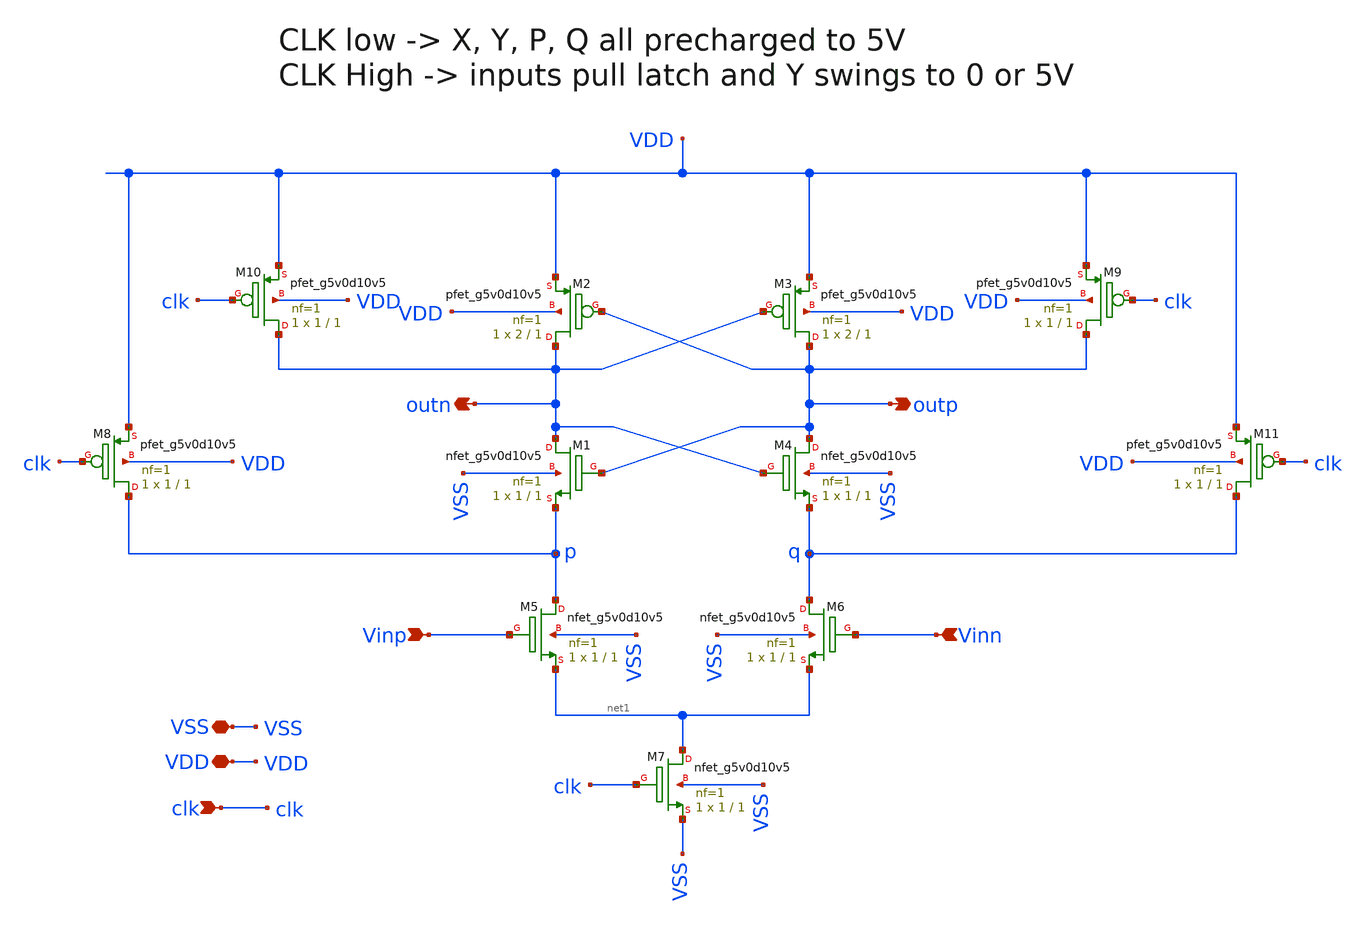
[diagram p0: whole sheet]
** sch_path: ADC/4bit_C2C/MagicAndSpice/strongarm_comp.sch
**.subckt strongarm_comp Vinp Vinn clk VDD outp outn VSS
*.ipin Vinp
*.ipin Vinn
*.ipin clk
*.iopin VDD
*.opin outp
*.opin outn
*.iopin VSS
XM1 outn outp p VSS sky130_fd_pr__nfet_g5v0d10v5 L=1 W=1 nf=1 ad='int((nf+1)/2) * W/nf * 0.29' as='int((nf+2)/2) * W/nf * 0.29'
+ pd='2*int((nf+1)/2) * (W/nf + 0.29)' ps='2*int((nf+2)/2) * (W/nf + 0.29)' nrd='0.29 / W' nrs='0.29 / W'
+ sa=0 sb=0 sd=0 mult=1 m=1
XM2 outn outp VDD VDD sky130_fd_pr__pfet_g5v0d10v5 L=1 W=2 nf=1 ad='int((nf+1)/2) * W/nf * 0.29' as='int((nf+2)/2) * W/nf * 0.29'
+ pd='2*int((nf+1)/2) * (W/nf + 0.29)' ps='2*int((nf+2)/2) * (W/nf + 0.29)' nrd='0.29 / W' nrs='0.29 / W'
+ sa=0 sb=0 sd=0 mult=1 m=1
XM3 outp outn VDD VDD sky130_fd_pr__pfet_g5v0d10v5 L=1 W=2 nf=1 ad='int((nf+1)/2) * W/nf * 0.29' as='int((nf+2)/2) * W/nf * 0.29'
+ pd='2*int((nf+1)/2) * (W/nf + 0.29)' ps='2*int((nf+2)/2) * (W/nf + 0.29)' nrd='0.29 / W' nrs='0.29 / W'
+ sa=0 sb=0 sd=0 mult=1 m=1
XM4 outp outn q VSS sky130_fd_pr__nfet_g5v0d10v5 L=1 W=1 nf=1 ad='int((nf+1)/2) * W/nf * 0.29' as='int((nf+2)/2) * W/nf * 0.29'
+ pd='2*int((nf+1)/2) * (W/nf + 0.29)' ps='2*int((nf+2)/2) * (W/nf + 0.29)' nrd='0.29 / W' nrs='0.29 / W'
+ sa=0 sb=0 sd=0 mult=1 m=1
XM5 p Vinp net1 VSS sky130_fd_pr__nfet_g5v0d10v5 L=1 W=1 nf=1 ad='int((nf+1)/2) * W/nf * 0.29' as='int((nf+2)/2) * W/nf * 0.29'
+ pd='2*int((nf+1)/2) * (W/nf + 0.29)' ps='2*int((nf+2)/2) * (W/nf + 0.29)' nrd='0.29 / W' nrs='0.29 / W'
+ sa=0 sb=0 sd=0 mult=1 m=1
XM6 q Vinn net1 VSS sky130_fd_pr__nfet_g5v0d10v5 L=1 W=1 nf=1 ad='int((nf+1)/2) * W/nf * 0.29' as='int((nf+2)/2) * W/nf * 0.29'
+ pd='2*int((nf+1)/2) * (W/nf + 0.29)' ps='2*int((nf+2)/2) * (W/nf + 0.29)' nrd='0.29 / W' nrs='0.29 / W'
+ sa=0 sb=0 sd=0 mult=1 m=1
XM7 net1 clk VSS VSS sky130_fd_pr__nfet_g5v0d10v5 L=1 W=1 nf=1 ad='int((nf+1)/2) * W/nf * 0.29' as='int((nf+2)/2) * W/nf * 0.29'
+ pd='2*int((nf+1)/2) * (W/nf + 0.29)' ps='2*int((nf+2)/2) * (W/nf + 0.29)' nrd='0.29 / W' nrs='0.29 / W'
+ sa=0 sb=0 sd=0 mult=1 m=1
XM9 outp clk VDD VDD sky130_fd_pr__pfet_g5v0d10v5 L=1 W=1 nf=1 ad='int((nf+1)/2) * W/nf * 0.29' as='int((nf+2)/2) * W/nf * 0.29'
+ pd='2*int((nf+1)/2) * (W/nf + 0.29)' ps='2*int((nf+2)/2) * (W/nf + 0.29)' nrd='0.29 / W' nrs='0.29 / W'
+ sa=0 sb=0 sd=0 mult=1 m=1
XM10 outn clk VDD VDD sky130_fd_pr__pfet_g5v0d10v5 L=1 W=1 nf=1 ad='int((nf+1)/2) * W/nf * 0.29' as='int((nf+2)/2) * W/nf * 0.29'
+ pd='2*int((nf+1)/2) * (W/nf + 0.29)' ps='2*int((nf+2)/2) * (W/nf + 0.29)' nrd='0.29 / W' nrs='0.29 / W'
+ sa=0 sb=0 sd=0 mult=1 m=1
XM8 p clk VDD VDD sky130_fd_pr__pfet_g5v0d10v5 L=1 W=1 nf=1 ad='int((nf+1)/2) * W/nf * 0.29' as='int((nf+2)/2) * W/nf * 0.29'
+ pd='2*int((nf+1)/2) * (W/nf + 0.29)' ps='2*int((nf+2)/2) * (W/nf + 0.29)' nrd='0.29 / W' nrs='0.29 / W'
+ sa=0 sb=0 sd=0 mult=1 m=1
XM11 q clk VDD VDD sky130_fd_pr__pfet_g5v0d10v5 L=1 W=1 nf=1 ad='int((nf+1)/2) * W/nf * 0.29' as='int((nf+2)/2) * W/nf * 0.29'
+ pd='2*int((nf+1)/2) * (W/nf + 0.29)' ps='2*int((nf+2)/2) * (W/nf + 0.29)' nrd='0.29 / W' nrs='0.29 / W'
+ sa=0 sb=0 sd=0 mult=1 m=1
**** begin user architecture code

** opencircuitdesign pdks install
.lib $::SKYWATER_MODELS/sky130.lib.spice tt


**** end user architecture code
**.ends
.end
